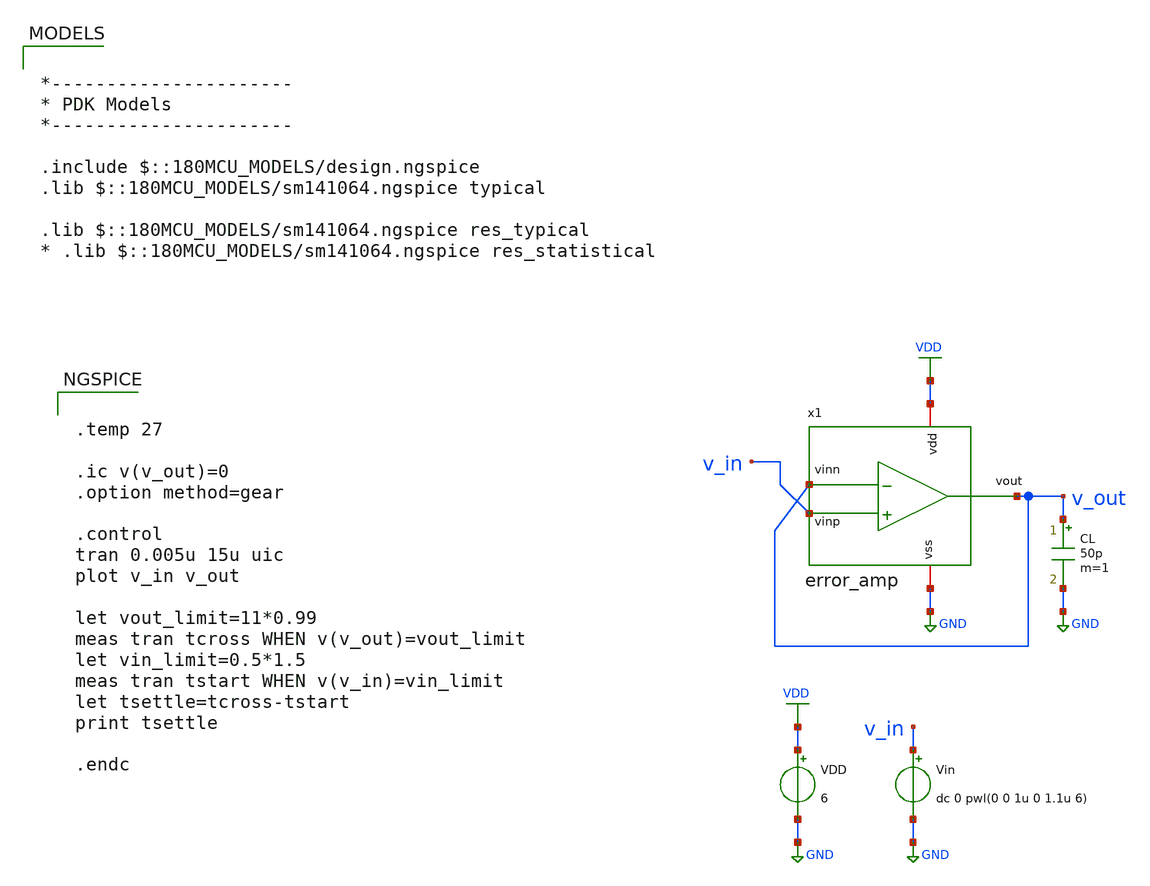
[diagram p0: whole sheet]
** sch_path: analog-db/drawings/ldo-005-ti-ldo-buffer-ref/gf180/error_amp/error_amp_tb-tran.sch
**.subckt error_amp_tb-tran
VDD VDD GND 6
Vin v_in GND dc 0 pwl(0 0 1u 0 1.1u 6)
CL v_out GND 50p m=1
x1 VDD v_out v_in v_out GND error_amp
**** begin user architecture code

*----------------------
* PDK Models
*----------------------

.include $::180MCU_MODELS/design.ngspice
.lib $::180MCU_MODELS/sm141064.ngspice typical

.lib $::180MCU_MODELS/sm141064.ngspice res_typical
* .lib $::180MCU_MODELS/sm141064.ngspice res_statistical



.temp 27

.ic v(v_out)=0
.option method=gear

.control
tran 0.005u 15u uic
plot v_in v_out

let vout_limit=11*0.99
meas tran tcross WHEN v(v_out)=vout_limit
let vin_limit=0.5*1.5
meas tran tstart WHEN v(v_in)=vin_limit
let tsettle=tcross-tstart
print tsettle

.endc

**** end user architecture code
**.ends

* expanding   symbol:  ldo-005-ti-ldo-buffer-ref/gf180/error_amp/error_amp.sym # of pins=5
** sym_path: analog-db/circuits/amp_032_ti_ldo_error_selfbias/pdk/gf180mcu/schematic/error_amp.sym
** sch_path: analog-db/circuits/amp_032_ti_ldo_error_selfbias/pdk/gf180mcu/schematic/error_amp.sch
.subckt error_amp vdd vout vinp vinn vss
*.iopin vdd
*.iopin vss
*.ipin vinp
*.opin vout
*.ipin vinn
XM2 net_b vinp net_c vss nfet_06v0 L=0.7u W=68.542u nf=1 ad='int((nf+1)/2) * W/nf * 0.18u' as='int((nf+2)/2) * W/nf * 0.18u'
+ pd='2*int((nf+1)/2) * (W/nf + 0.18u)' ps='2*int((nf+2)/2) * (W/nf + 0.18u)' nrd='0.18u / W' nrs='0.18u / W'
+ sa=0 sb=0 sd=0 m=1
XM3m net_a net_d vdd vdd pfet_06v0 L=0.5u W=69.545u nf=1 ad='int((nf+1)/2) * W/nf * 0.18u' as='int((nf+2)/2) * W/nf * 0.18u'
+ pd='2*int((nf+1)/2) * (W/nf + 0.18u)' ps='2*int((nf+2)/2) * (W/nf + 0.18u)' nrd='0.18u / W' nrs='0.18u / W'
+ sa=0 sb=0 sd=0 m=1
XM4 net_f net_a net_d vdd pfet_06v0 L=0.5u W=10u nf=1 ad='int((nf+1)/2) * W/nf * 0.18u' as='int((nf+2)/2) * W/nf * 0.18u'
+ pd='2*int((nf+1)/2) * (W/nf + 0.18u)' ps='2*int((nf+2)/2) * (W/nf + 0.18u)' nrd='0.18u / W' nrs='0.18u / W'
+ sa=0 sb=0 sd=0 m=1
XM5 net_b net_d vdd vdd pfet_06v0 L=0.5u W=69.545u nf=1 ad='int((nf+1)/2) * W/nf * 0.18u' as='int((nf+2)/2) * W/nf * 0.18u'
+ pd='2*int((nf+1)/2) * (W/nf + 0.18u)' ps='2*int((nf+2)/2) * (W/nf + 0.18u)' nrd='0.18u / W' nrs='0.18u / W'
+ sa=0 sb=0 sd=0 m=1
XM6 vout net_b vdd vdd pfet_06v0 L=3.8349u W=20u nf=1 ad='int((nf+1)/2) * W/nf * 0.18u' as='int((nf+2)/2) * W/nf * 0.18u'
+ pd='2*int((nf+1)/2) * (W/nf + 0.18u)' ps='2*int((nf+2)/2) * (W/nf + 0.18u)' nrd='0.18u / W' nrs='0.18u / W'
+ sa=0 sb=0 sd=0 m=1
Cc net1 vout 6.7168p m=1
XRZ net_b net1 vdd ppolyf_u_3k r_width=1u r_length=9.476u m=1
XM1 net_a vinn net_c vss nfet_06v0 L=0.7u W=68.542u nf=1 ad='int((nf+1)/2) * W/nf * 0.18u' as='int((nf+2)/2) * W/nf * 0.18u'
+ pd='2*int((nf+1)/2) * (W/nf + 0.18u)' ps='2*int((nf+2)/2) * (W/nf + 0.18u)' nrd='0.18u / W' nrs='0.18u / W'
+ sa=0 sb=0 sd=0 m=1
XM_mirror_error_amp_ref net2 net2 vss vss nfet_06v0 L=2u W=34.533u nf=1 ad='int((nf+1)/2) * W/nf * 0.18u'
+ as='int((nf+2)/2) * W/nf * 0.18u' pd='2*int((nf+1)/2) * (W/nf + 0.18u)' ps='2*int((nf+2)/2) * (W/nf + 0.18u)'
+ nrd='0.18u / W' nrs='0.18u / W' sa=0 sb=0 sd=0 m=1
XM_mirror_f net_f net2 vss vss nfet_06v0 L=2u W=5u nf=1 ad='int((nf+1)/2) * W/nf * 0.18u' as='int((nf+2)/2) * W/nf * 0.18u'
+ pd='2*int((nf+1)/2) * (W/nf + 0.18u)' ps='2*int((nf+2)/2) * (W/nf + 0.18u)' nrd='0.18u / W' nrs='0.18u / W'
+ sa=0 sb=0 sd=0 m=1
XM_mirror_c net_c net2 vss vss nfet_06v0 L=2u W=34.533u nf=1 ad='int((nf+1)/2) * W/nf * 0.18u' as='int((nf+2)/2) * W/nf * 0.18u'
+ pd='2*int((nf+1)/2) * (W/nf + 0.18u)' ps='2*int((nf+2)/2) * (W/nf + 0.18u)' nrd='0.18u / W' nrs='0.18u / W'
+ sa=0 sb=0 sd=0 m=1
XM_mirror_ea_out vout net2 vss vss nfet_06v0 L=2u W=34.533u nf=1 ad='int((nf+1)/2) * W/nf * 0.18u' as='int((nf+2)/2) * W/nf * 0.18u'
+ pd='2*int((nf+1)/2) * (W/nf + 0.18u)' ps='2*int((nf+2)/2) * (W/nf + 0.18u)' nrd='0.18u / W' nrs='0.18u / W'
+ sa=0 sb=0 sd=0 m=1
XM_bias net2 net2 vdd vdd pfet_06v0 L=2u W=6.3111u nf=1 ad='int((nf+1)/2) * W/nf * 0.18u' as='int((nf+2)/2) * W/nf * 0.18u'
+ pd='2*int((nf+1)/2) * (W/nf + 0.18u)' ps='2*int((nf+2)/2) * (W/nf + 0.18u)' nrd='0.18u / W' nrs='0.18u / W'
+ sa=0 sb=0 sd=0 m=1
.ends

.GLOBAL VDD
.GLOBAL GND
.end
